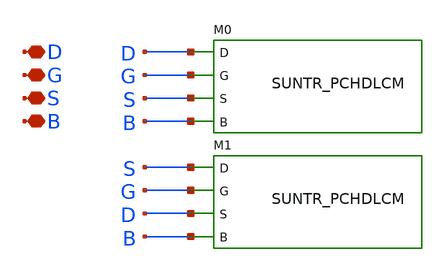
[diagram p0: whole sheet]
** sch_path: ip/sun_tr_sky130nm/design/SUN_TR_SKY130NM/SUNTR_PCHDLCM2.sch
**.subckt SUNTR_PCHDLCM2 D G S B
*.iopin D
*.iopin G
*.iopin S
*.iopin B
M0 D G S B SUNTR_PCHDLCM
M1 S G D B SUNTR_PCHDLCM
**.ends
.end
